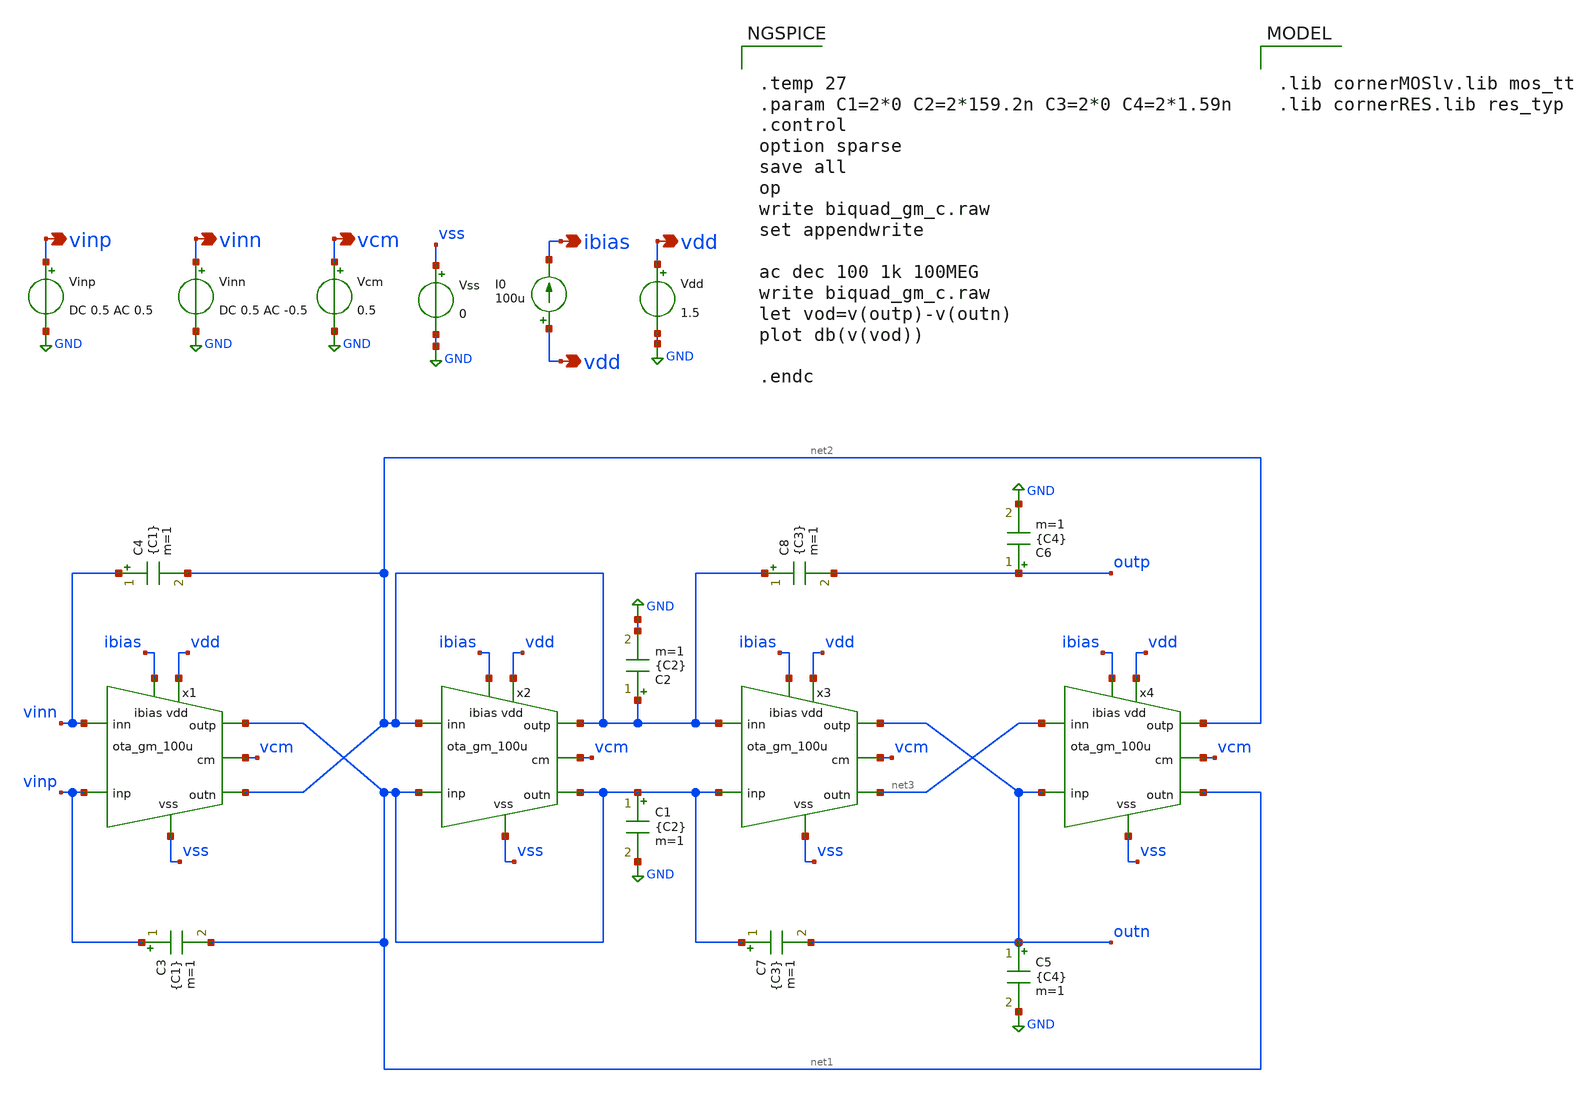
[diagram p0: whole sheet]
** sch_path: 3_Real_Cir/biquad_gm_c.sch
**.subckt biquad_gm_c vinp vinn vcm ibias vdd vdd
*.opin vinp
*.opin vinn
*.opin vcm
*.opin ibias
*.opin vdd
*.opin vdd
Vinp vinp GND DC 0.5 AC 0.5
Vinn vinn GND DC 0.5 AC -0.5
Vcm vcm GND 0.5
x1 vinp vinn net1 net2 vcm vdd vss ibias ota_gm_100u
C3 vinp net1 {C1} m=1
x2 net1 net2 net2 net1 vcm vdd vss ibias ota_gm_100u
x3 net1 net2 outn net3 vcm vdd vss ibias ota_gm_100u
x4 outn net3 net2 net1 vcm vdd vss ibias ota_gm_100u
C6 outp GND {C4} m=1
C8 net2 outp {C3} m=1
C4 vinn net2 {C1} m=1
C2 net2 GND {C2} m=1
C7 net1 outn {C3} m=1
C5 outn GND {C4} m=1
C1 net1 GND {C2} m=1
Vss vss GND 0
I0 vdd ibias 100u
Vdd vdd GND 1.5
**** begin user architecture code


.temp 27
.param C1=2*0 C2=2*159.2n C3=2*0 C4=2*1.59n
.control
option sparse
save all
op
write biquad_gm_c.raw
set appendwrite

ac dec 100 1k 100MEG
write biquad_gm_c.raw
let vod=v(outp)-v(outn)
plot db(v(vod))

.endc



.lib cornerMOSlv.lib mos_tt
.lib cornerRES.lib res_typ

**** end user architecture code
**.ends

* expanding   symbol:  ota_gm_100u.sym # of pins=8
** sym_path: 3_Real_Cir/ota_gm_100u.sym
** sch_path: 3_Real_Cir/ota_gm_100u.sch
.subckt ota_gm_100u inp inn outp outn cm vdd vss ibias
*.ipin inp
*.ipin inn
*.opin outp
*.opin outn
*.iopin vdd
*.ipin ibias
*.ipin cm
*.iopin vss
XM3 net3 net3 vdd vdd sg13_lv_pmos w=1.4u l=0.28u ng=1 m=1 mm_ok=1
XM4 net3 net3 vdd vdd sg13_lv_pmos w=1.4u l=0.28u ng=1 m=1 mm_ok=1
XM1 outn inp net2 vss sg13_lv_nmos w=2.8u l=0.28u ng=1 m=1 mm_ok=1
XM2 outp inn net2 vss sg13_lv_nmos w=2.8u l=0.28u ng=1 m=1 mm_ok=1
XM11 net2 net4 net1 vss sg13_lv_nmos w=0.5u l=5u ng=1 m=1 mm_ok=1
XM8 outp net3 vdd vdd sg13_lv_pmos w=1.4u l=0.28u ng=1 m=1 mm_ok=1
XM7 outn net3 vdd vdd sg13_lv_pmos w=1.4u l=0.28u ng=1 m=1 mm_ok=1
XM5 net3 cm net2 vss sg13_lv_nmos w=2.8u l=0.28u ng=1 m=1 mm_ok=1
XM6 net3 cm net2 vss sg13_lv_nmos w=2u l=2.8u ng=1 m=1 mm_ok=1
XM12 net1 ibias vss vss sg13_lv_nmos w=0.5u l=0.13u ng=1 m=1 mm_ok=1
XM9 ibias net4 net5 vss sg13_lv_nmos w=0.5u l=0.13u ng=1 m=1 mm_ok=1
XM10 net5 ibias vss vss sg13_lv_nmos w=0.5u l=0.13u ng=1 m=1 mm_ok=1
.ends

.GLOBAL GND
.end
